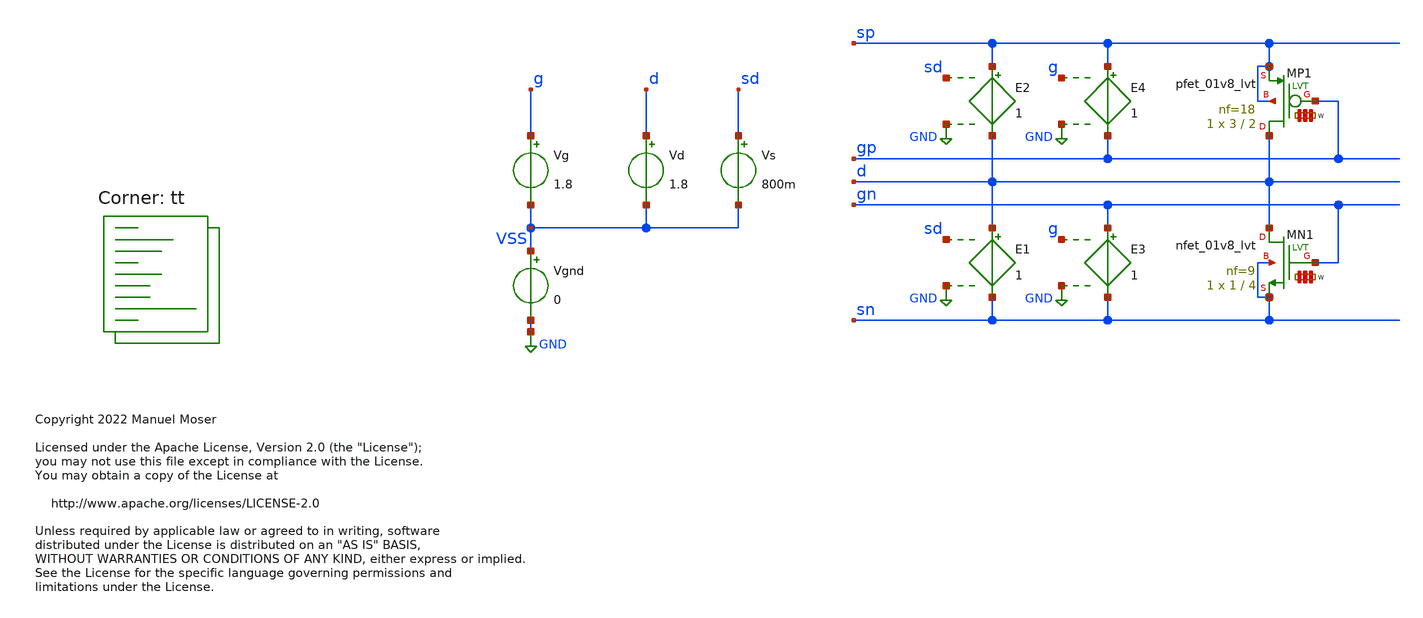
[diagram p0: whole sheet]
** sch_path: xschem/gmid.sch
* Copyright 2022 Manuel Moser
* Licensed under the Apache License, Version 2.0 (the "License");
**.subckt gmid
Vg g VSS 1.8
Vgnd VSS GND 0
Vd d VSS 1.8
Vs sd VSS 800m
XMN1 d gn sn sn sky130_fd_pr__nfet_01v8_lvt L=4 W='1 * 9 ' nf=9 ad='int((nf+1)/2) * W / nf * 0.29' as='int((nf+2)/2) * W / nf * 0.29'
+ pd='2*int((nf+1)/2) * (W / nf + 0.29)' ps='2*int((nf+2)/2) * (W / nf + 0.29)' nrd='0.29 / W ' nrs='0.29 / W '
+ sa=0 sb=0 sd=0 mult=1 m=1
XMP1 d gp sp sp sky130_fd_pr__pfet_01v8_lvt L=2 W='3 * 18 ' nf=18 ad='int((nf+1)/2) * W / nf * 0.29'
+ as='int((nf+2)/2) * W / nf * 0.29' pd='2*int((nf+1)/2) * (W / nf + 0.29)' ps='2*int((nf+2)/2) * (W / nf + 0.29)'
+ nrd='0.29 / W ' nrs='0.29 / W ' sa=0 sb=0 sd=0 mult=1 m=1
E1 d sn sd GND 1
E2 sp d sd GND 1
E3 gn sn g GND 1
E4 sp gp g GND 1
**** begin user architecture code



.temp 27
.options savecurrents
.options gmin = 1e-15

.save all
.options savecurrents

.control
	dc VG 0 1 1m
	let vgs = abs(v(g))

	let idn  = abs(@m.xmn1.msky130_fd_pr__nfet_01v8_lvt[id])
	let gmn  = abs(deriv(idn)/deriv(vgs))
	let gmidn = gmn/(idn)

	let idp  = abs(@m.xmp1.msky130_fd_pr__pfet_01v8_lvt[id])
	let gmp  = abs(deriv(idp)/deriv(vgs))
	let gmidp = gmp/(idp)

	plot gmidp vs idp gmidn vs idn xlog


.endc




.lib $::SKYWATER_MODELS/sky130.lib.spice tt
**** end user architecture code
**.ends
.GLOBAL GND
.end
